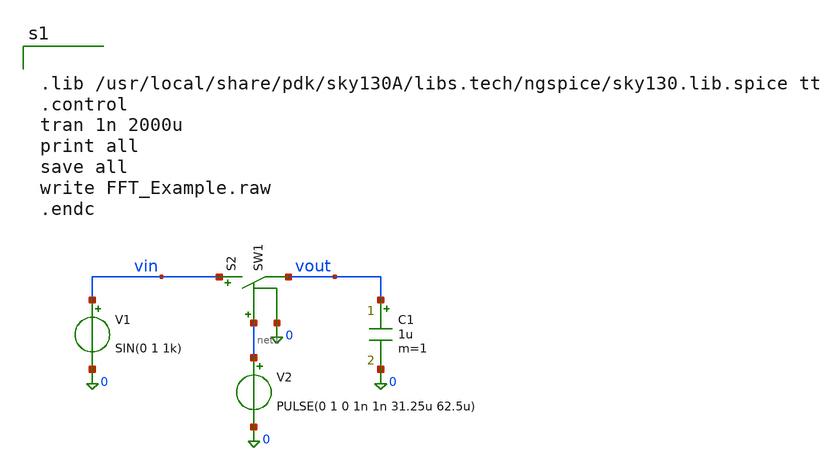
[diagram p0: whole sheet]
** sch_path: mag/FFT_Example.sch
**.subckt FFT_Example
V1 vin 0 SIN(0 1 1k)
C1 vout 0 1u m=1
S2 vin vout net1 0 SW1
V2 net1 0 PULSE(0 1 0 1n 1n 31.25u 62.5u)
**** begin user architecture code


.lib /usr/local/share/pdk/sky130A/libs.tech/ngspice/sky130.lib.spice tt
.control
tran 1n 2000u
print all
save all
write FFT_Example.raw
.endc

**** end user architecture code
**.ends
**** begin user architecture code
.MODEL SW1 SW   VT=0.9 VH=0.01  RON=0.01 ROFF=10G
**** end user architecture code
.end
